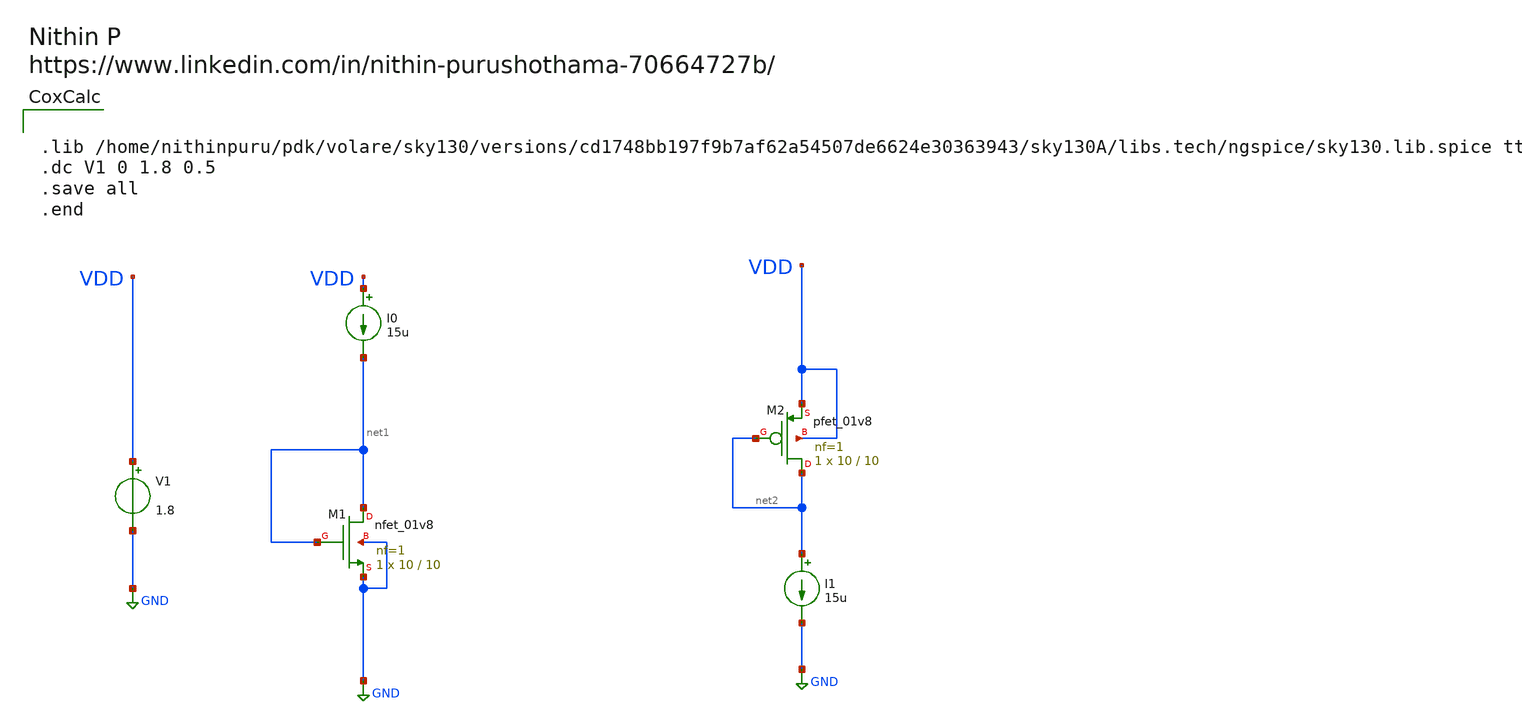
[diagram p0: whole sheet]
** sch_path: Schematics/μCox Calculation of PMOS and NMOS/CoxCalc.sch
**.subckt CoxCalc
XM1 net1 net1 GND GND sky130_fd_pr__nfet_01v8 L=10 W=10 nf=1 ad='int((nf+1)/2) * W/nf * 0.29' as='int((nf+2)/2) * W/nf * 0.29'
+ pd='2*int((nf+1)/2) * (W/nf + 0.29)' ps='2*int((nf+2)/2) * (W/nf + 0.29)' nrd='0.29 / W' nrs='0.29 / W'
+ sa=0 sb=0 sd=0 mult=1 m=1
V1 VDD GND 1.8
I0 VDD net1 15u
XM2 net2 net2 VDD VDD sky130_fd_pr__pfet_01v8 L=10 W=10 nf=1 ad='int((nf+1)/2) * W/nf * 0.29' as='int((nf+2)/2) * W/nf * 0.29'
+ pd='2*int((nf+1)/2) * (W/nf + 0.29)' ps='2*int((nf+2)/2) * (W/nf + 0.29)' nrd='0.29 / W' nrs='0.29 / W'
+ sa=0 sb=0 sd=0 mult=1 m=1
I1 net2 GND 15u
**** begin user architecture code


.lib /home/nithinpuru/pdk/volare/sky130/versions/cd1748bb197f9b7af62a54507de6624e30363943/sky130A/libs.tech/ngspice/sky130.lib.spice tt
.dc V1 0 1.8 0.5
.save all
.end

**** end user architecture code
**.ends
.GLOBAL GND
.end
